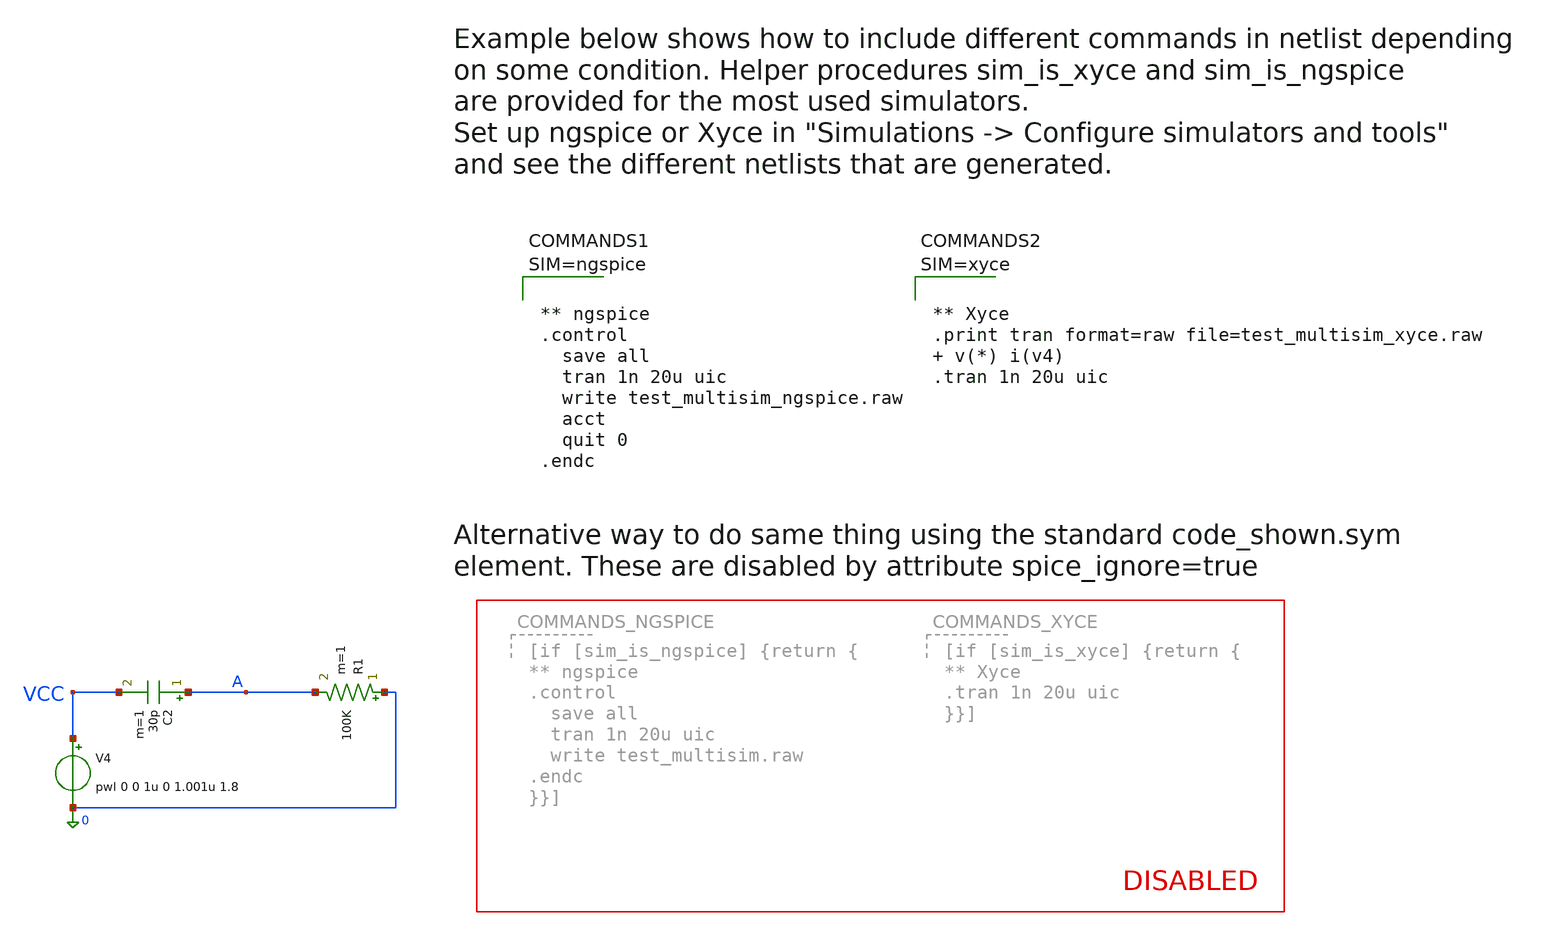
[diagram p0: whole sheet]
** sch_path: sky130A/xschem_libs/sky130_tests/test_multisim/schematic/test_multisim.sch
* Copyright 2021 Stefan Frederik Schippers
* Licensed under the Apache License, Version 2.0 (the "License");
* you may not use this file except in compliance with the License.
* You may obtain a copy of the License at
* https://www.apache.org/licenses/LICENSE-2.0
* Unless required by applicable law or agreed to in writing, software
* distributed under the License is distributed on an "AS IS" BASIS,
* WITHOUT WARRANTIES OR CONDITIONS OF ANY KIND, either express or implied.
* See the License for the specific language governing permissions and
* limitations under the License.
**.subckt test_multisim
V4 VCC 0 pwl 0 0 1u 0 1.001u 1.8
R1 0 A 100K m=1
C2 A VCC 30p m=1
**** begin user architecture code



** ngspice
.control
  save all
  tran 1n 20u uic
  write test_multisim_ngspice.raw
  acct
  quit 0
.endc






**** end user architecture code
**.ends
.end
